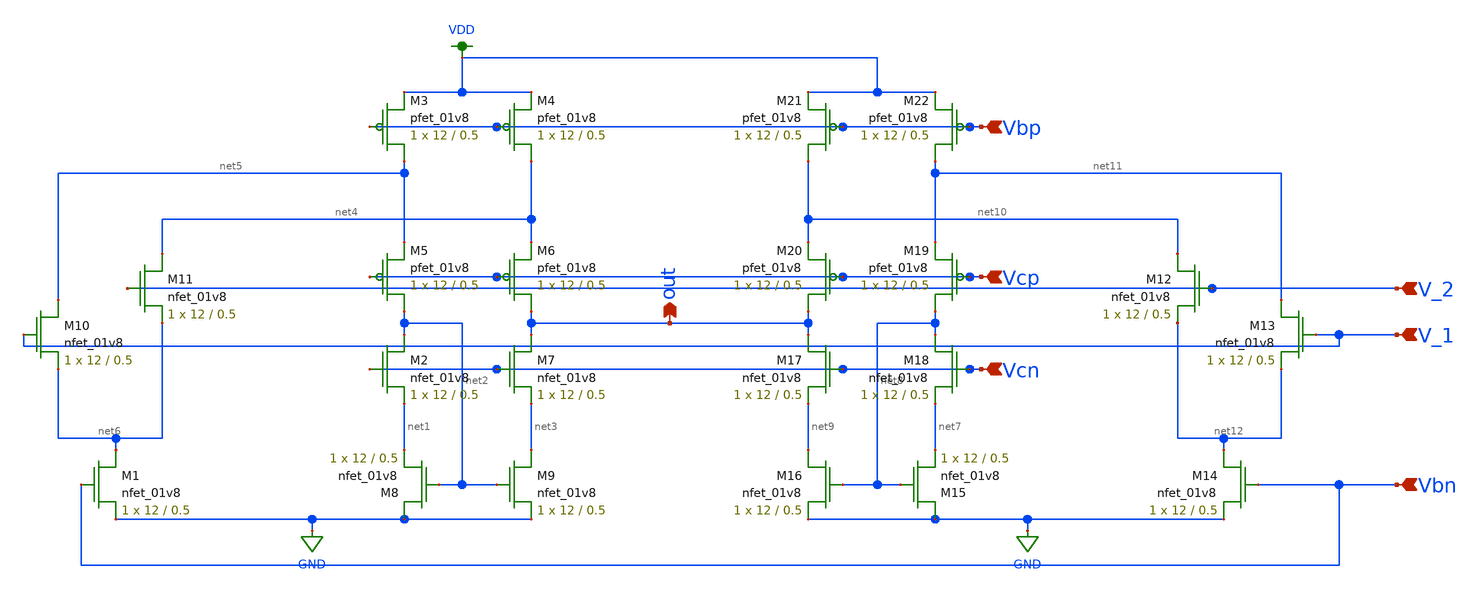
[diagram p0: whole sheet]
** sch_path: miniproject3/LVS_FCDA.sch
**.subckt LVS_FCDA V_1 V_2 Vcp Vcn out Vbp Vbn
*.ipin V_1
*.ipin V_2
*.ipin Vcp
*.ipin Vcn
*.opin out
*.ipin Vbp
*.ipin Vbn
XM11 net4 V_2 net6 GND sky130_fd_pr__nfet_01v8 L=0.5 W=12 nf=1 ad='int((nf+1)/2) * W/nf * 0.29' as='int((nf+2)/2) * W/nf * 0.29'
+ pd='2*int((nf+1)/2) * (W/nf + 0.29)' ps='2*int((nf+2)/2) * (W/nf + 0.29)' nrd='0.29 / W' nrs='0.29 / W'
+ sa=0 sb=0 sd=0 mult=1 m=1
XM10 net5 V_1 net6 GND sky130_fd_pr__nfet_01v8 L=0.5 W=12 nf=1 ad='int((nf+1)/2) * W/nf * 0.29' as='int((nf+2)/2) * W/nf * 0.29'
+ pd='2*int((nf+1)/2) * (W/nf + 0.29)' ps='2*int((nf+2)/2) * (W/nf + 0.29)' nrd='0.29 / W' nrs='0.29 / W'
+ sa=0 sb=0 sd=0 mult=1 m=1
XM1 net6 Vbn GND GND sky130_fd_pr__nfet_01v8 L=0.5 W=12 nf=1 ad='int((nf+1)/2) * W/nf * 0.29' as='int((nf+2)/2) * W/nf * 0.29'
+ pd='2*int((nf+1)/2) * (W/nf + 0.29)' ps='2*int((nf+2)/2) * (W/nf + 0.29)' nrd='0.29 / W' nrs='0.29 / W'
+ sa=0 sb=0 sd=0 mult=1 m=1
XM8 GND net2 net1 GND sky130_fd_pr__nfet_01v8 L=0.5 W=12 nf=1 ad='int((nf+1)/2) * W/nf * 0.29' as='int((nf+2)/2) * W/nf * 0.29'
+ pd='2*int((nf+1)/2) * (W/nf + 0.29)' ps='2*int((nf+2)/2) * (W/nf + 0.29)' nrd='0.29 / W' nrs='0.29 / W'
+ sa=0 sb=0 sd=0 mult=1 m=1
XM9 net3 net2 GND GND sky130_fd_pr__nfet_01v8 L=0.5 W=12 nf=1 ad='int((nf+1)/2) * W/nf * 0.29' as='int((nf+2)/2) * W/nf * 0.29'
+ pd='2*int((nf+1)/2) * (W/nf + 0.29)' ps='2*int((nf+2)/2) * (W/nf + 0.29)' nrd='0.29 / W' nrs='0.29 / W'
+ sa=0 sb=0 sd=0 mult=1 m=1
XM7 out Vcn net3 GND sky130_fd_pr__nfet_01v8 L=0.5 W=12 nf=1 ad='int((nf+1)/2) * W/nf * 0.29' as='int((nf+2)/2) * W/nf * 0.29'
+ pd='2*int((nf+1)/2) * (W/nf + 0.29)' ps='2*int((nf+2)/2) * (W/nf + 0.29)' nrd='0.29 / W' nrs='0.29 / W'
+ sa=0 sb=0 sd=0 mult=1 m=1
XM2 net2 Vcn net1 GND sky130_fd_pr__nfet_01v8 L=0.5 W=12 nf=1 ad='int((nf+1)/2) * W/nf * 0.29' as='int((nf+2)/2) * W/nf * 0.29'
+ pd='2*int((nf+1)/2) * (W/nf + 0.29)' ps='2*int((nf+2)/2) * (W/nf + 0.29)' nrd='0.29 / W' nrs='0.29 / W'
+ sa=0 sb=0 sd=0 mult=1 m=1
XM5 net2 Vcp net5 VDD sky130_fd_pr__pfet_01v8 L=0.5 W=12 nf=1 ad='int((nf+1)/2) * W/nf * 0.29' as='int((nf+2)/2) * W/nf * 0.29'
+ pd='2*int((nf+1)/2) * (W/nf + 0.29)' ps='2*int((nf+2)/2) * (W/nf + 0.29)' nrd='0.29 / W' nrs='0.29 / W'
+ sa=0 sb=0 sd=0 mult=1 m=1
XM6 out Vcp net4 VDD sky130_fd_pr__pfet_01v8 L=0.5 W=12 nf=1 ad='int((nf+1)/2) * W/nf * 0.29' as='int((nf+2)/2) * W/nf * 0.29'
+ pd='2*int((nf+1)/2) * (W/nf + 0.29)' ps='2*int((nf+2)/2) * (W/nf + 0.29)' nrd='0.29 / W' nrs='0.29 / W'
+ sa=0 sb=0 sd=0 mult=1 m=1
XM4 net4 Vbp VDD VDD sky130_fd_pr__pfet_01v8 L=0.5 W=12 nf=1 ad='int((nf+1)/2) * W/nf * 0.29' as='int((nf+2)/2) * W/nf * 0.29'
+ pd='2*int((nf+1)/2) * (W/nf + 0.29)' ps='2*int((nf+2)/2) * (W/nf + 0.29)' nrd='0.29 / W' nrs='0.29 / W'
+ sa=0 sb=0 sd=0 mult=1 m=1
XM3 net5 Vbp VDD VDD sky130_fd_pr__pfet_01v8 L=0.5 W=12 nf=1 ad='int((nf+1)/2) * W/nf * 0.29' as='int((nf+2)/2) * W/nf * 0.29'
+ pd='2*int((nf+1)/2) * (W/nf + 0.29)' ps='2*int((nf+2)/2) * (W/nf + 0.29)' nrd='0.29 / W' nrs='0.29 / W'
+ sa=0 sb=0 sd=0 mult=1 m=1
XM12 net10 V_2 net12 GND sky130_fd_pr__nfet_01v8 L=0.5 W=12 nf=1 ad='int((nf+1)/2) * W/nf * 0.29' as='int((nf+2)/2) * W/nf * 0.29'
+ pd='2*int((nf+1)/2) * (W/nf + 0.29)' ps='2*int((nf+2)/2) * (W/nf + 0.29)' nrd='0.29 / W' nrs='0.29 / W'
+ sa=0 sb=0 sd=0 mult=1 m=1
XM13 net11 V_1 net12 GND sky130_fd_pr__nfet_01v8 L=0.5 W=12 nf=1 ad='int((nf+1)/2) * W/nf * 0.29' as='int((nf+2)/2) * W/nf * 0.29'
+ pd='2*int((nf+1)/2) * (W/nf + 0.29)' ps='2*int((nf+2)/2) * (W/nf + 0.29)' nrd='0.29 / W' nrs='0.29 / W'
+ sa=0 sb=0 sd=0 mult=1 m=1
XM14 net12 Vbn GND GND sky130_fd_pr__nfet_01v8 L=0.5 W=12 nf=1 ad='int((nf+1)/2) * W/nf * 0.29' as='int((nf+2)/2) * W/nf * 0.29'
+ pd='2*int((nf+1)/2) * (W/nf + 0.29)' ps='2*int((nf+2)/2) * (W/nf + 0.29)' nrd='0.29 / W' nrs='0.29 / W'
+ sa=0 sb=0 sd=0 mult=1 m=1
XM15 GND net8 net7 GND sky130_fd_pr__nfet_01v8 L=0.5 W=12 nf=1 ad='int((nf+1)/2) * W/nf * 0.29' as='int((nf+2)/2) * W/nf * 0.29'
+ pd='2*int((nf+1)/2) * (W/nf + 0.29)' ps='2*int((nf+2)/2) * (W/nf + 0.29)' nrd='0.29 / W' nrs='0.29 / W'
+ sa=0 sb=0 sd=0 mult=1 m=1
XM16 net9 net8 GND GND sky130_fd_pr__nfet_01v8 L=0.5 W=12 nf=1 ad='int((nf+1)/2) * W/nf * 0.29' as='int((nf+2)/2) * W/nf * 0.29'
+ pd='2*int((nf+1)/2) * (W/nf + 0.29)' ps='2*int((nf+2)/2) * (W/nf + 0.29)' nrd='0.29 / W' nrs='0.29 / W'
+ sa=0 sb=0 sd=0 mult=1 m=1
XM17 out Vcn net9 GND sky130_fd_pr__nfet_01v8 L=0.5 W=12 nf=1 ad='int((nf+1)/2) * W/nf * 0.29' as='int((nf+2)/2) * W/nf * 0.29'
+ pd='2*int((nf+1)/2) * (W/nf + 0.29)' ps='2*int((nf+2)/2) * (W/nf + 0.29)' nrd='0.29 / W' nrs='0.29 / W'
+ sa=0 sb=0 sd=0 mult=1 m=1
XM18 net8 Vcn net7 GND sky130_fd_pr__nfet_01v8 L=0.5 W=12 nf=1 ad='int((nf+1)/2) * W/nf * 0.29' as='int((nf+2)/2) * W/nf * 0.29'
+ pd='2*int((nf+1)/2) * (W/nf + 0.29)' ps='2*int((nf+2)/2) * (W/nf + 0.29)' nrd='0.29 / W' nrs='0.29 / W'
+ sa=0 sb=0 sd=0 mult=1 m=1
XM19 net8 Vcp net11 VDD sky130_fd_pr__pfet_01v8 L=0.5 W=12 nf=1 ad='int((nf+1)/2) * W/nf * 0.29' as='int((nf+2)/2) * W/nf * 0.29'
+ pd='2*int((nf+1)/2) * (W/nf + 0.29)' ps='2*int((nf+2)/2) * (W/nf + 0.29)' nrd='0.29 / W' nrs='0.29 / W'
+ sa=0 sb=0 sd=0 mult=1 m=1
XM20 out Vcp net10 VDD sky130_fd_pr__pfet_01v8 L=0.5 W=12 nf=1 ad='int((nf+1)/2) * W/nf * 0.29' as='int((nf+2)/2) * W/nf * 0.29'
+ pd='2*int((nf+1)/2) * (W/nf + 0.29)' ps='2*int((nf+2)/2) * (W/nf + 0.29)' nrd='0.29 / W' nrs='0.29 / W'
+ sa=0 sb=0 sd=0 mult=1 m=1
XM21 net10 Vbp VDD VDD sky130_fd_pr__pfet_01v8 L=0.5 W=12 nf=1 ad='int((nf+1)/2) * W/nf * 0.29' as='int((nf+2)/2) * W/nf * 0.29'
+ pd='2*int((nf+1)/2) * (W/nf + 0.29)' ps='2*int((nf+2)/2) * (W/nf + 0.29)' nrd='0.29 / W' nrs='0.29 / W'
+ sa=0 sb=0 sd=0 mult=1 m=1
XM22 net11 Vbp VDD VDD sky130_fd_pr__pfet_01v8 L=0.5 W=12 nf=1 ad='int((nf+1)/2) * W/nf * 0.29' as='int((nf+2)/2) * W/nf * 0.29'
+ pd='2*int((nf+1)/2) * (W/nf + 0.29)' ps='2*int((nf+2)/2) * (W/nf + 0.29)' nrd='0.29 / W' nrs='0.29 / W'
+ sa=0 sb=0 sd=0 mult=1 m=1
**.ends
.GLOBAL VDD
.GLOBAL GND
.end
